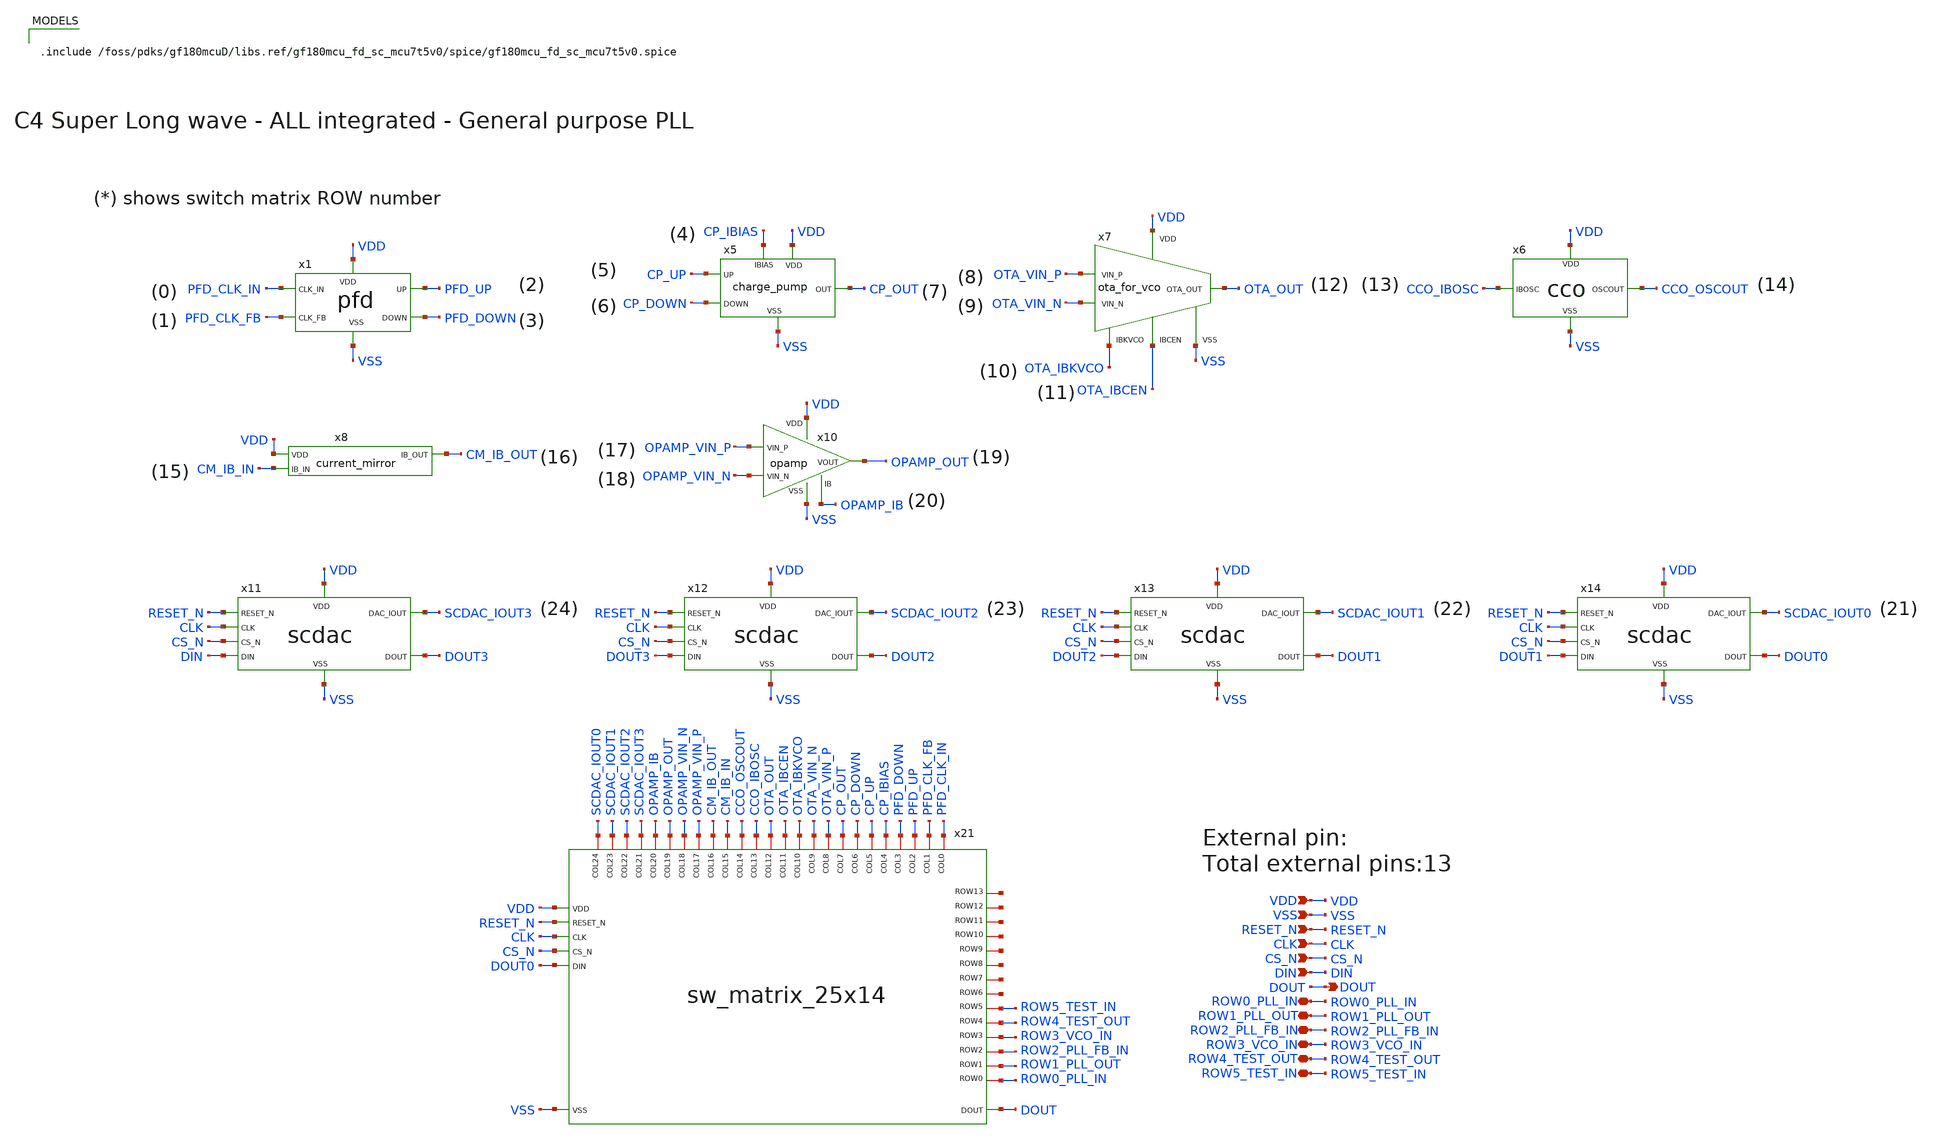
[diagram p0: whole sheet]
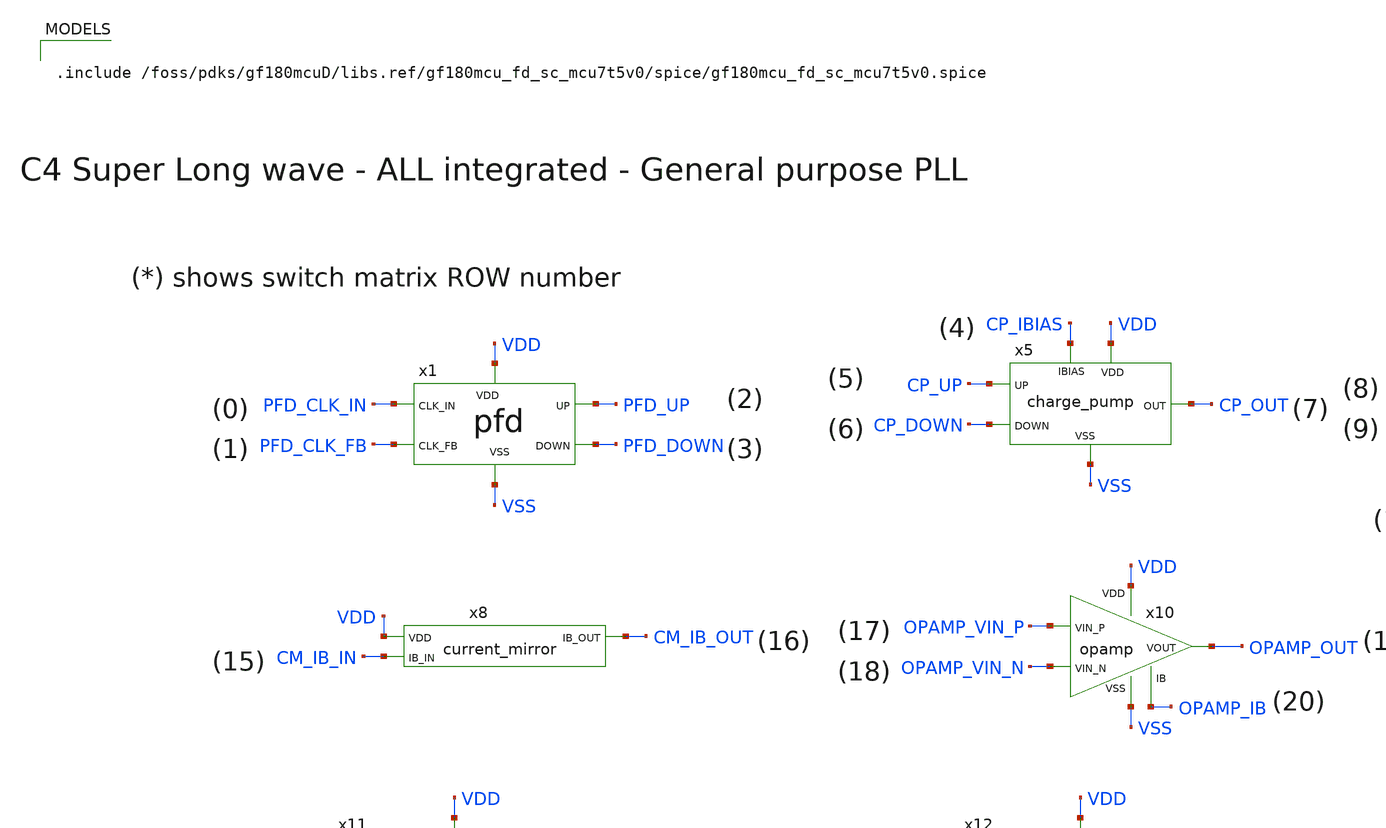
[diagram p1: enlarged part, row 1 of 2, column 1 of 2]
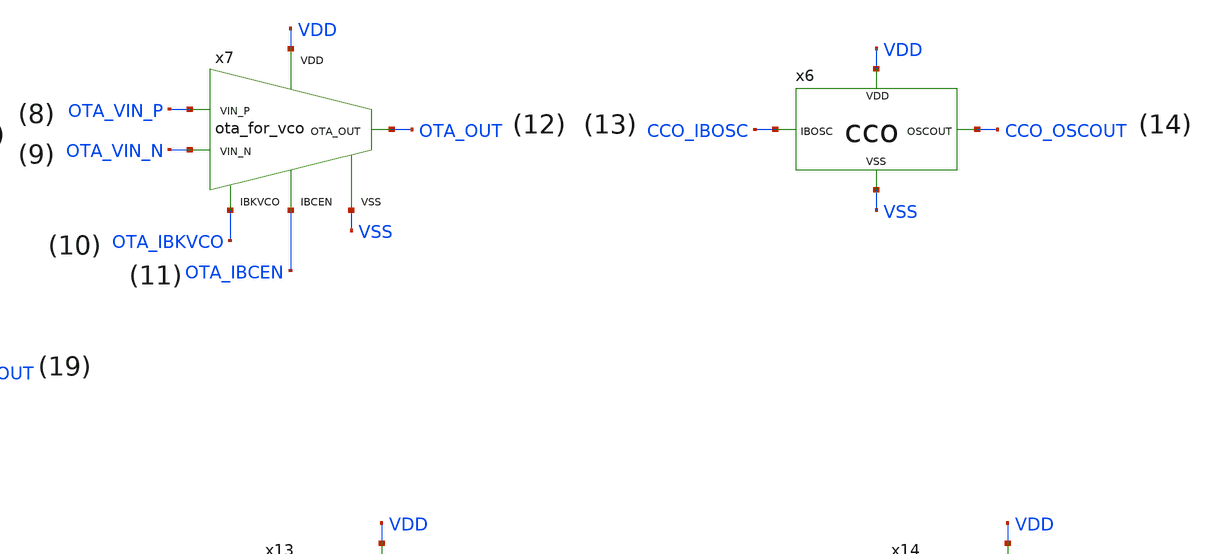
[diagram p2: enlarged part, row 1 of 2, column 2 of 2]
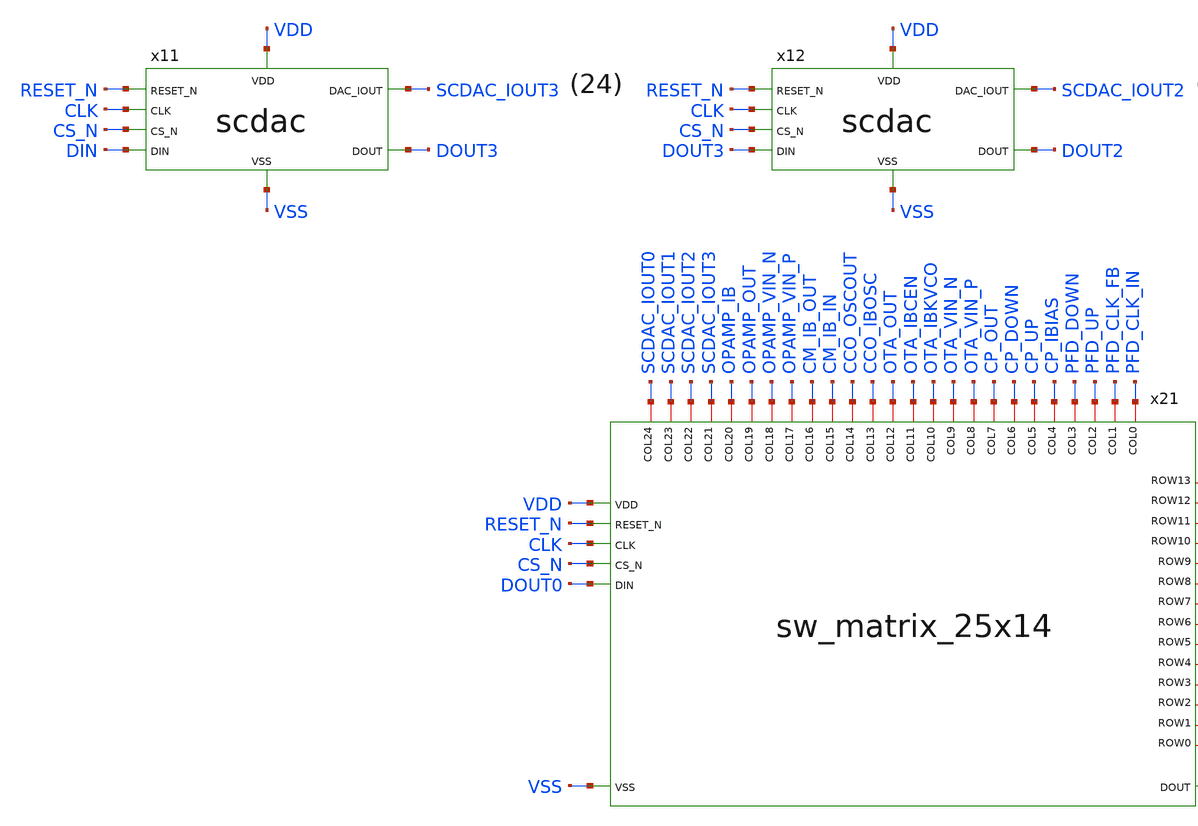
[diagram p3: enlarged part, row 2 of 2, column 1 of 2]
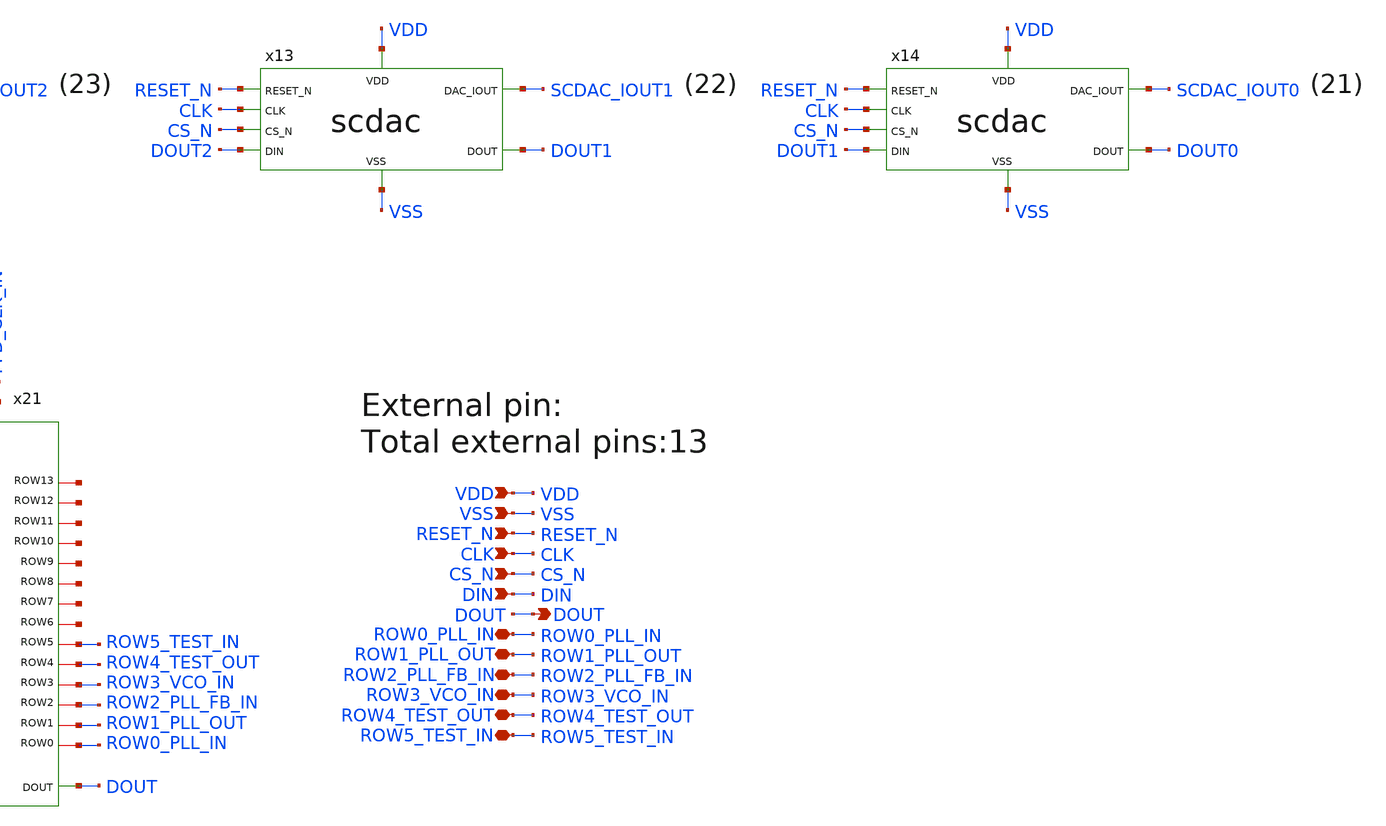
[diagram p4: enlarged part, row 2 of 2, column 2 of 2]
** sch_path: designs/libs/core_analog/c4_all/c4_all.sch
* Copyright 2022 GlobalFoundries PDK Authors
* Licensed under the Apache License, Version 2.0 (the "License");
* you may not use this file except in compliance with the License.
* You may obtain a copy of the License at
* https://www.apache.org/licenses/LICENSE-2.0
* Unless required by applicable law or agreed to in writing, software
* distributed under the License is distributed on an "AS IS" BASIS,
* WITHOUT WARRANTIES OR CONDITIONS OF ANY KIND, either express or implied.
* See the License for the specific language governing permissions and
* limitations under the License.
**.subckt c4_all VDD VSS RESET_N CLK CS_N DIN ROW0_PLL_IN ROW1_PLL_OUT ROW3_VCO_IN ROW4_TEST_OUT
*+ ROW5_TEST_IN DOUT ROW2_PLL_FB_IN
*.ipin VDD
*.ipin VSS
*.ipin RESET_N
*.ipin CLK
*.ipin CS_N
*.ipin DIN
*.iopin ROW0_PLL_IN
*.iopin ROW1_PLL_OUT
*.iopin ROW3_VCO_IN
*.iopin ROW4_TEST_OUT
*.iopin ROW5_TEST_IN
*.opin DOUT
*.iopin ROW2_PLL_FB_IN
x5 VDD VSS CP_UP CP_DOWN CP_OUT CP_IBIAS charge_pump
x6 VDD VSS CCO_IBOSC CCO_OSCOUT cco
x7 OTA_IBKVCO OTA_VIN_N OTA_VIN_P OTA_OUT VSS VDD OTA_IBCEN ota_for_vco
x8 VDD CM_IB_IN CM_IB_OUT current_mirror
x10 VDD VSS OPAMP_IB OPAMP_OUT OPAMP_VIN_P OPAMP_VIN_N opamp
x21 VDD VSS RESET_N CLK CS_N DOUT0 DOUT PFD_CLK_IN PFD_CLK_FB PFD_UP PFD_DOWN CP_IBIAS CP_UP CP_DOWN
+ CP_OUT OTA_VIN_P OTA_VIN_N OTA_IBKVCO OTA_IBCEN OTA_OUT CCO_IBOSC CCO_OSCOUT CM_IB_IN CM_IB_OUT
+ OPAMP_VIN_P OPAMP_VIN_N OPAMP_OUT OPAMP_IB SCDAC_IOUT3 SCDAC_IOUT2 SCDAC_IOUT1 SCDAC_IOUT0 ROW0_PLL_IN
+ ROW1_PLL_OUT ROW2_PLL_FB_IN ROW3_VCO_IN ROW4_TEST_OUT ROW5_TEST_IN net1 net2 net3 net4 net5 net6 net7 net8
+ sw_matrix_25x14
x1 PFD_UP PFD_CLK_IN PFD_CLK_FB PFD_DOWN VSS VDD pfd
x11 VDD VSS RESET_N CLK DIN CS_N DOUT3 SCDAC_IOUT3 scdac
x12 VDD VSS RESET_N CLK DOUT3 CS_N DOUT2 SCDAC_IOUT2 scdac
x13 VDD VSS RESET_N CLK DOUT2 CS_N DOUT1 SCDAC_IOUT1 scdac
x14 VDD VSS RESET_N CLK DOUT1 CS_N DOUT0 SCDAC_IOUT0 scdac
**** begin user architecture code

.include /foss/pdks/gf180mcuD/libs.ref/gf180mcu_fd_sc_mcu7t5v0/spice/gf180mcu_fd_sc_mcu7t5v0.spice


**** end user architecture code
**.ends
.end
